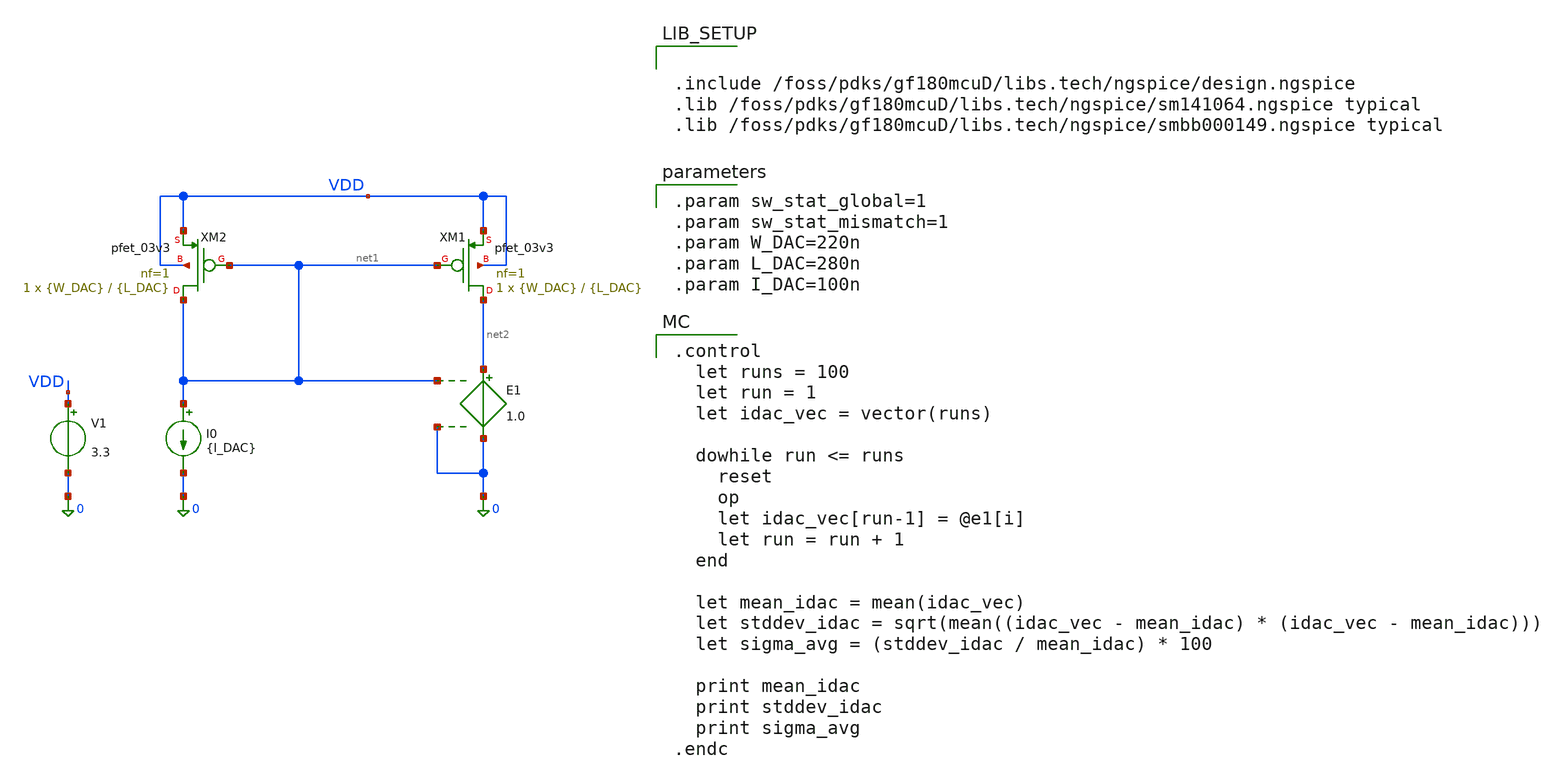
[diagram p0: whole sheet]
** sch_path: lab_2/lab2.sch
**.subckt lab2
I0 net1 0 {I_DAC}
E1 net2 0 net1 0 1.0
V1 VDD 0 3.3
XM1 net2 net1 VDD VDD pfet_03v3 L={L_DAC} W={W_DAC} nf=1 ad='int((nf+1)/2) * W/nf * 0.18u' as='int((nf+2)/2) * W/nf * 0.18u'
+ pd='2*int((nf+1)/2) * (W/nf + 0.18u)' ps='2*int((nf+2)/2) * (W/nf + 0.18u)' nrd='0.18u / W' nrs='0.18u / W'
+ sa=0 sb=0 sd=0 m=1
XM2 net1 net1 VDD VDD pfet_03v3 L={L_DAC} W={W_DAC} nf=1 ad='int((nf+1)/2) * W/nf * 0.18u' as='int((nf+2)/2) * W/nf * 0.18u'
+ pd='2*int((nf+1)/2) * (W/nf + 0.18u)' ps='2*int((nf+2)/2) * (W/nf + 0.18u)' nrd='0.18u / W' nrs='0.18u / W'
+ sa=0 sb=0 sd=0 m=1
**** begin user architecture code


.include /foss/pdks/gf180mcuD/libs.tech/ngspice/design.ngspice
.lib /foss/pdks/gf180mcuD/libs.tech/ngspice/sm141064.ngspice typical
.lib /foss/pdks/gf180mcuD/libs.tech/ngspice/smbb000149.ngspice typical



.param sw_stat_global=1
.param sw_stat_mismatch=1
.param W_DAC=220n
.param L_DAC=280n
.param I_DAC=100n



.control
  let runs = 100
  let run = 1
  let idac_vec = vector(runs)

  dowhile run <= runs
    reset
    op
    let idac_vec[run-1] = @e1[i]
    let run = run + 1
  end

  let mean_idac = mean(idac_vec)
  let stddev_idac = sqrt(mean((idac_vec - mean_idac) * (idac_vec - mean_idac)))
  let sigma_avg = (stddev_idac / mean_idac) * 100

  print mean_idac
  print stddev_idac
  print sigma_avg
.endc

**** end user architecture code
**.ends
.end
